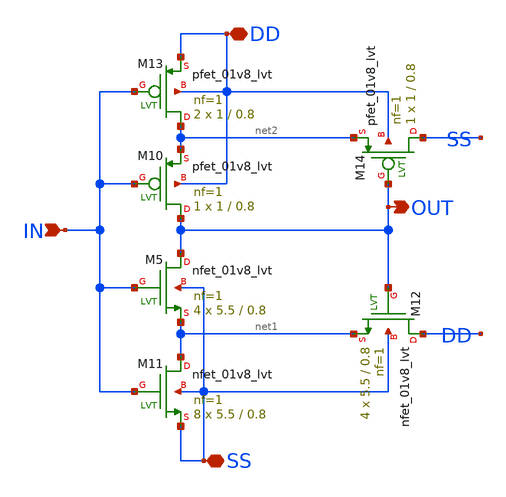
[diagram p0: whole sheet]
** sch_path: xschem/st_inv.sch
**.subckt st_inv IN DD SS OUT
*.ipin IN
*.iopin DD
*.iopin SS
*.opin OUT
XM5 OUT IN net1 SS sky130_fd_pr__nfet_01v8_lvt L=0.8 W=5.5 nf=1 ad='int((nf+1)/2) * W/nf * 0.29' as='int((nf+2)/2) * W/nf * 0.29'
+ pd='2*int((nf+1)/2) * (W/nf + 0.29)' ps='2*int((nf+2)/2) * (W/nf + 0.29)' nrd='0.29 / W' nrs='0.29 / W'
+ sa=0 sb=0 sd=0 mult=4 m=4
XM10 OUT IN net2 DD sky130_fd_pr__pfet_01v8_lvt L=0.8 W=1 nf=1 ad='int((nf+1)/2) * W/nf * 0.29' as='int((nf+2)/2) * W/nf * 0.29'
+ pd='2*int((nf+1)/2) * (W/nf + 0.29)' ps='2*int((nf+2)/2) * (W/nf + 0.29)' nrd='0.29 / W' nrs='0.29 / W'
+ sa=0 sb=0 sd=0 mult=1 m=1
XM11 net1 IN SS SS sky130_fd_pr__nfet_01v8_lvt L=0.8 W=5.5 nf=1 ad='int((nf+1)/2) * W/nf * 0.29' as='int((nf+2)/2) * W/nf * 0.29'
+ pd='2*int((nf+1)/2) * (W/nf + 0.29)' ps='2*int((nf+2)/2) * (W/nf + 0.29)' nrd='0.29 / W' nrs='0.29 / W'
+ sa=0 sb=0 sd=0 mult=8 m=8
XM12 DD OUT net1 SS sky130_fd_pr__nfet_01v8_lvt L=0.8 W=5.5 nf=1 ad='int((nf+1)/2) * W/nf * 0.29' as='int((nf+2)/2) * W/nf * 0.29'
+ pd='2*int((nf+1)/2) * (W/nf + 0.29)' ps='2*int((nf+2)/2) * (W/nf + 0.29)' nrd='0.29 / W' nrs='0.29 / W'
+ sa=0 sb=0 sd=0 mult=4 m=4
XM13 net2 IN DD DD sky130_fd_pr__pfet_01v8_lvt L=0.8 W=1 nf=1 ad='int((nf+1)/2) * W/nf * 0.29' as='int((nf+2)/2) * W/nf * 0.29'
+ pd='2*int((nf+1)/2) * (W/nf + 0.29)' ps='2*int((nf+2)/2) * (W/nf + 0.29)' nrd='0.29 / W' nrs='0.29 / W'
+ sa=0 sb=0 sd=0 mult=2 m=2
XM14 SS OUT net2 DD sky130_fd_pr__pfet_01v8_lvt L=0.8 W=1 nf=1 ad='int((nf+1)/2) * W/nf * 0.29' as='int((nf+2)/2) * W/nf * 0.29'
+ pd='2*int((nf+1)/2) * (W/nf + 0.29)' ps='2*int((nf+2)/2) * (W/nf + 0.29)' nrd='0.29 / W' nrs='0.29 / W'
+ sa=0 sb=0 sd=0 mult=1 m=1
**.ends
.end
